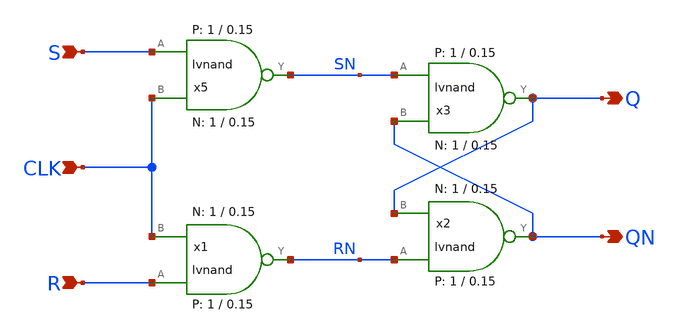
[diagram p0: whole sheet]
** sch_path: sky130A/xschem_libs/sky130_tests_ase/srlatch/schematic/srlatch.sch
* Copyright 2021 Stefan Frederik Schippers
* Licensed under the Apache License, Version 2.0 (the "License");
* you may not use this file except in compliance with the License.
* You may obtain a copy of the License at
* https://www.apache.org/licenses/LICENSE-2.0
* Unless required by applicable law or agreed to in writing, software
* distributed under the License is distributed on an "AS IS" BASIS,
* WITHOUT WARRANTIES OR CONDITIONS OF ANY KIND, either express or implied.
* See the License for the specific language governing permissions and
* limitations under the License.
**.subckt srlatch S R Q QN CLK
*.ipin S
*.ipin R
*.opin Q
*.opin QN
*.ipin CLK
x5 S CLK SN VCC VSS lvnand WidthN=1 LenN=0.15 WidthP=1 LenP=0.15 m=1
x1 R CLK RN VCC VSS lvnand WidthN=1 LenN=0.15 WidthP=1 LenP=0.15 m=1
x2 RN Q QN VCC VSS lvnand WidthN=1 LenN=0.15 WidthP=1 LenP=0.15 m=1
x3 SN QN Q VCC VSS lvnand WidthN=1 LenN=0.15 WidthP=1 LenP=0.15 m=1
**.ends
**** begin user architecture code


vd d 0 0
vg g 0 0


**** end user architecture code
.end
